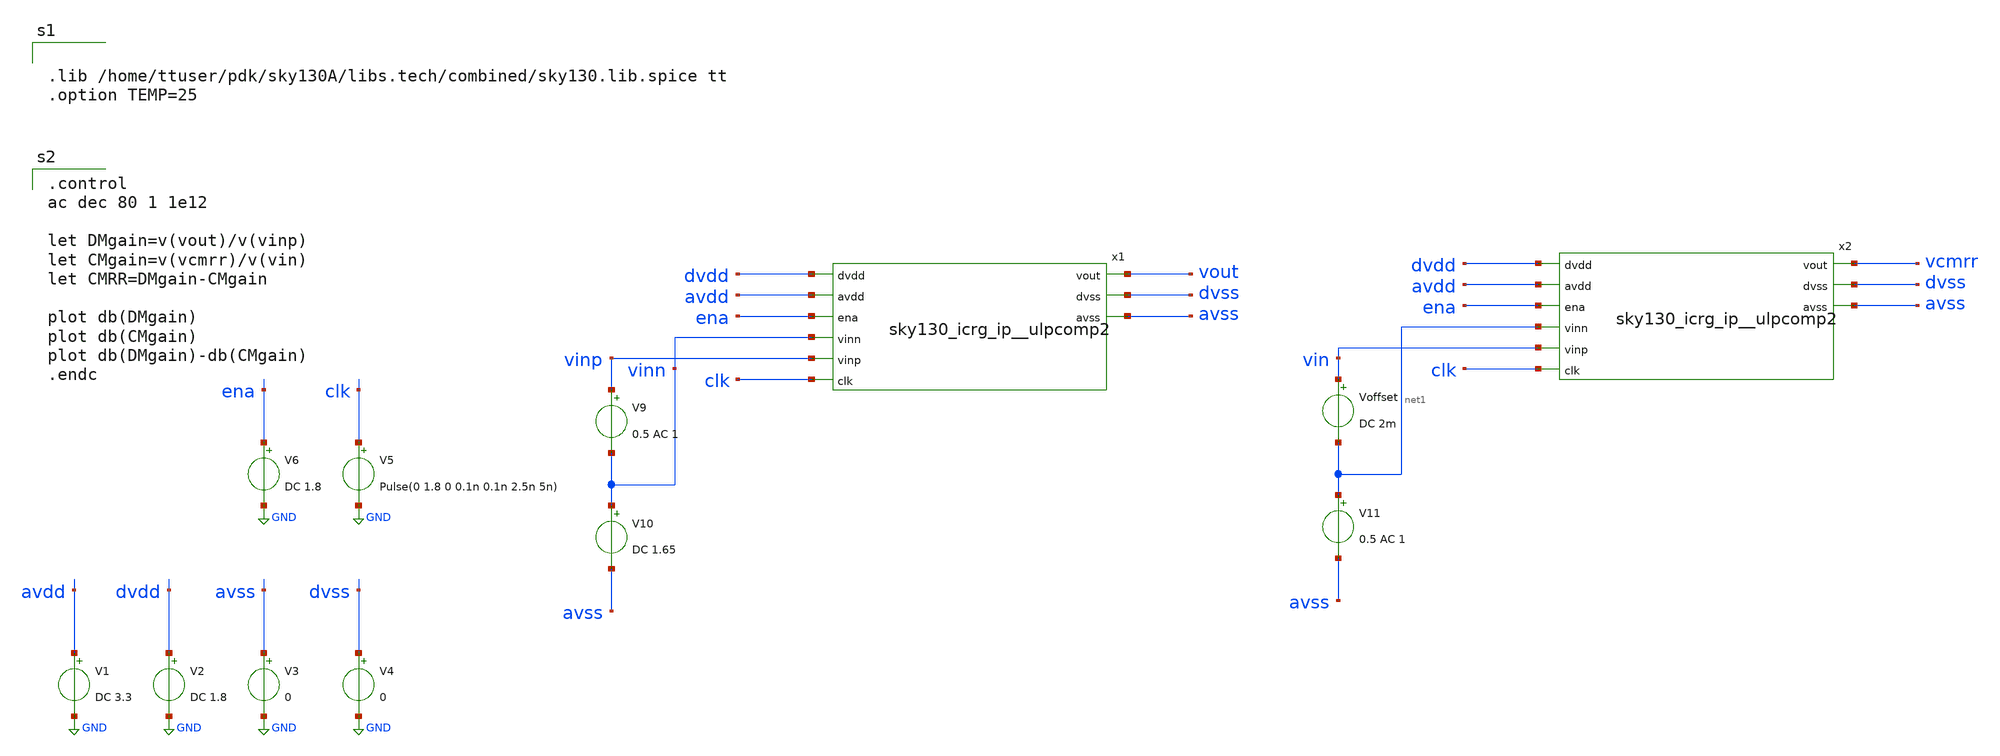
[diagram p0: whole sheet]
** sch_path: xschem/CMRR_tb.sch
**.subckt CMRR_tb
x1 dvdd avdd ena vout vinn vinp clk dvss avss sky130_icrg_ip__ulpcomp2
V1 avdd GND DC 3.3
V2 dvdd GND DC 1.8
V3 avss GND 0
V4 dvss GND 0
V5 clk GND Pulse(0 1.8 0 0.1n 0.1n 2.5n 5n)
V6 ena GND DC 1.8
V9 vinp vinn 0.5 AC 1
V10 vinn avss DC 1.65
x2 dvdd avdd ena vcmrr net1 vin clk dvss avss sky130_icrg_ip__ulpcomp2
V11 net1 avss 0.5 AC 1
Voffset vin net1 DC 2m
**** begin user architecture code


.lib /home/ttuser/pdk/sky130A/libs.tech/combined/sky130.lib.spice tt
.option TEMP=25


.control
ac dec 80 1 1e12

let DMgain=v(vout)/v(vinp)
let CMgain=v(vcmrr)/v(vin)
let CMRR=DMgain-CMgain

plot db(DMgain)
plot db(CMgain)
plot db(DMgain)-db(CMgain)
.endc

**** end user architecture code
**.ends

* expanding   symbol:  sky130_icrg_ip__ulpcomp2.sym # of pins=9
** sym_path: xschem/sky130_icrg_ip__ulpcomp2.sym
** sch_path: xschem/sky130_icrg_ip__ulpcomp2.sch
.subckt sky130_icrg_ip__ulpcomp2 dvdd avdd ena vout vinn vinp clk dvss avss
*.ipin avdd
*.ipin vinp
*.ipin vinn
*.opin avss
*.opin vout
*.opin dvss
*.ipin dvdd
*.ipin clk
*.ipin ena
XM1 net1 clka net3 net3 sky130_fd_pr__pfet_g5v0d10v5 L=0.5 W=3 nf=1 ad='int((nf+1)/2) * W/nf * 0.29'
+ as='int((nf+2)/2) * W/nf * 0.29' pd='2*int((nf+1)/2) * (W/nf + 0.29)' ps='2*int((nf+2)/2) * (W/nf + 0.29)'
+ nrd='0.29 / W' nrs='0.29 / W' sa=0 sb=0 sd=0 mult=1 m=1
XM2 oneg vinp net1 net1 sky130_fd_pr__pfet_g5v0d10v5 L=0.5 W=3 nf=1 ad='int((nf+1)/2) * W/nf * 0.29'
+ as='int((nf+2)/2) * W/nf * 0.29' pd='2*int((nf+1)/2) * (W/nf + 0.29)' ps='2*int((nf+2)/2) * (W/nf + 0.29)'
+ nrd='0.29 / W' nrs='0.29 / W' sa=0 sb=0 sd=0 mult=1 m=1
XM3 opos vinn net1 net1 sky130_fd_pr__pfet_g5v0d10v5 L=0.5 W=3 nf=1 ad='int((nf+1)/2) * W/nf * 0.29'
+ as='int((nf+2)/2) * W/nf * 0.29' pd='2*int((nf+1)/2) * (W/nf + 0.29)' ps='2*int((nf+2)/2) * (W/nf + 0.29)'
+ nrd='0.29 / W' nrs='0.29 / W' sa=0 sb=0 sd=0 mult=1 m=1
XM7 oneg clka net2 net2 sky130_fd_pr__nfet_03v3_nvt L=0.5 W=3 nf=1 ad='int((nf+1)/2) * W/nf * 0.29' as='int((nf+2)/2) * W/nf * 0.29'
+ pd='2*int((nf+1)/2) * (W/nf + 0.29)' ps='2*int((nf+2)/2) * (W/nf + 0.29)' nrd='0.29 / W' nrs='0.29 / W'
+ sa=0 sb=0 sd=0 mult=1 m=1
XM5 opos clka net2 net2 sky130_fd_pr__nfet_03v3_nvt L=0.5 W=3 nf=1 ad='int((nf+1)/2) * W/nf * 0.29' as='int((nf+2)/2) * W/nf * 0.29'
+ pd='2*int((nf+1)/2) * (W/nf + 0.29)' ps='2*int((nf+2)/2) * (W/nf + 0.29)' nrd='0.29 / W' nrs='0.29 / W'
+ sa=0 sb=0 sd=0 mult=1 m=1
XM6 clka clk dvss dvss sky130_fd_pr__nfet_01v8 L=0.15 W=1 nf=1 ad='int((nf+1)/2) * W/nf * 0.29' as='int((nf+2)/2) * W/nf * 0.29'
+ pd='2*int((nf+1)/2) * (W/nf + 0.29)' ps='2*int((nf+2)/2) * (W/nf + 0.29)' nrd='0.29 / W' nrs='0.29 / W'
+ sa=0 sb=0 sd=0 mult=1 m=1
XM8 clka clk dvddb dvddb sky130_fd_pr__pfet_01v8 L=0.15 W=1 nf=1 ad='int((nf+1)/2) * W/nf * 0.29' as='int((nf+2)/2) * W/nf * 0.29'
+ pd='2*int((nf+1)/2) * (W/nf + 0.29)' ps='2*int((nf+2)/2) * (W/nf + 0.29)' nrd='0.29 / W' nrs='0.29 / W'
+ sa=0 sb=0 sd=0 mult=1 m=1
XM9 net4 clkb dvddb dvddb sky130_fd_pr__pfet_01v8 L=0.15 W=1 nf=1 ad='int((nf+1)/2) * W/nf * 0.29' as='int((nf+2)/2) * W/nf * 0.29'
+ pd='2*int((nf+1)/2) * (W/nf + 0.29)' ps='2*int((nf+2)/2) * (W/nf + 0.29)' nrd='0.29 / W' nrs='0.29 / W'
+ sa=0 sb=0 sd=0 mult=1 m=1
XM10 net4 net5 dvddb dvddb sky130_fd_pr__pfet_01v8 L=0.15 W=1 nf=1 ad='int((nf+1)/2) * W/nf * 0.29' as='int((nf+2)/2) * W/nf * 0.29'
+ pd='2*int((nf+1)/2) * (W/nf + 0.29)' ps='2*int((nf+2)/2) * (W/nf + 0.29)' nrd='0.29 / W' nrs='0.29 / W'
+ sa=0 sb=0 sd=0 mult=1 m=1
XM11 net5 net4 dvddb dvddb sky130_fd_pr__pfet_01v8 L=0.15 W=1 nf=1 ad='int((nf+1)/2) * W/nf * 0.29' as='int((nf+2)/2) * W/nf * 0.29'
+ pd='2*int((nf+1)/2) * (W/nf + 0.29)' ps='2*int((nf+2)/2) * (W/nf + 0.29)' nrd='0.29 / W' nrs='0.29 / W'
+ sa=0 sb=0 sd=0 mult=1 m=1
XM12 net5 clkb dvddb dvddb sky130_fd_pr__pfet_01v8 L=0.15 W=1 nf=1 ad='int((nf+1)/2) * W/nf * 0.29' as='int((nf+2)/2) * W/nf * 0.29'
+ pd='2*int((nf+1)/2) * (W/nf + 0.29)' ps='2*int((nf+2)/2) * (W/nf + 0.29)' nrd='0.29 / W' nrs='0.29 / W'
+ sa=0 sb=0 sd=0 mult=1 m=1
XM13 net4 opos net6 dvss sky130_fd_pr__nfet_01v8 L=0.15 W=1 nf=1 ad='int((nf+1)/2) * W/nf * 0.29' as='int((nf+2)/2) * W/nf * 0.29'
+ pd='2*int((nf+1)/2) * (W/nf + 0.29)' ps='2*int((nf+2)/2) * (W/nf + 0.29)' nrd='0.29 / W' nrs='0.29 / W'
+ sa=0 sb=0 sd=0 mult=1 m=1
XM14 net5 oneg net7 dvss sky130_fd_pr__nfet_01v8 L=0.15 W=1 nf=1 ad='int((nf+1)/2) * W/nf * 0.29' as='int((nf+2)/2) * W/nf * 0.29'
+ pd='2*int((nf+1)/2) * (W/nf + 0.29)' ps='2*int((nf+2)/2) * (W/nf + 0.29)' nrd='0.29 / W' nrs='0.29 / W'
+ sa=0 sb=0 sd=0 mult=1 m=1
XM15 net6 net5 net8 dvss sky130_fd_pr__nfet_01v8 L=0.15 W=1 nf=1 ad='int((nf+1)/2) * W/nf * 0.29' as='int((nf+2)/2) * W/nf * 0.29'
+ pd='2*int((nf+1)/2) * (W/nf + 0.29)' ps='2*int((nf+2)/2) * (W/nf + 0.29)' nrd='0.29 / W' nrs='0.29 / W'
+ sa=0 sb=0 sd=0 mult=1 m=1
XM16 net7 net4 net8 dvss sky130_fd_pr__nfet_01v8 L=0.15 W=1 nf=1 ad='int((nf+1)/2) * W/nf * 0.29' as='int((nf+2)/2) * W/nf * 0.29'
+ pd='2*int((nf+1)/2) * (W/nf + 0.29)' ps='2*int((nf+2)/2) * (W/nf + 0.29)' nrd='0.29 / W' nrs='0.29 / W'
+ sa=0 sb=0 sd=0 mult=1 m=1
XM17 net8 clkb dvss dvss sky130_fd_pr__nfet_01v8 L=0.15 W=1 nf=1 ad='int((nf+1)/2) * W/nf * 0.29' as='int((nf+2)/2) * W/nf * 0.29'
+ pd='2*int((nf+1)/2) * (W/nf + 0.29)' ps='2*int((nf+2)/2) * (W/nf + 0.29)' nrd='0.29 / W' nrs='0.29 / W'
+ sa=0 sb=0 sd=0 mult=1 m=1
XM4 net2 net2 avss avss sky130_fd_pr__nfet_03v3_nvt L=0.5 W=3 nf=1 ad='int((nf+1)/2) * W/nf * 0.29' as='int((nf+2)/2) * W/nf * 0.29'
+ pd='2*int((nf+1)/2) * (W/nf + 0.29)' ps='2*int((nf+2)/2) * (W/nf + 0.29)' nrd='0.29 / W' nrs='0.29 / W'
+ sa=0 sb=0 sd=0 mult=1 m=1
XM18 vout net4 dvss dvss sky130_fd_pr__nfet_01v8 L=0.15 W=1 nf=1 ad='int((nf+1)/2) * W/nf * 0.29' as='int((nf+2)/2) * W/nf * 0.29'
+ pd='2*int((nf+1)/2) * (W/nf + 0.29)' ps='2*int((nf+2)/2) * (W/nf + 0.29)' nrd='0.29 / W' nrs='0.29 / W'
+ sa=0 sb=0 sd=0 mult=1 m=1
XM19 vout net4 dvdd dvdd sky130_fd_pr__pfet_01v8 L=0.15 W=1 nf=1 ad='int((nf+1)/2) * W/nf * 0.29' as='int((nf+2)/2) * W/nf * 0.29'
+ pd='2*int((nf+1)/2) * (W/nf + 0.29)' ps='2*int((nf+2)/2) * (W/nf + 0.29)' nrd='0.29 / W' nrs='0.29 / W'
+ sa=0 sb=0 sd=0 mult=1 m=1
XM20 avdd ena net3 avss sky130_fd_pr__nfet_03v3_nvt L=0.5 W=3 nf=1 ad='int((nf+1)/2) * W/nf * 0.29' as='int((nf+2)/2) * W/nf * 0.29'
+ pd='2*int((nf+1)/2) * (W/nf + 0.29)' ps='2*int((nf+2)/2) * (W/nf + 0.29)' nrd='0.29 / W' nrs='0.29 / W'
+ sa=0 sb=0 sd=0 mult=1 m=1
XM23 dvdd ena dvddb dvss sky130_fd_pr__nfet_01v8 L=0.15 W=1 nf=1 ad='int((nf+1)/2) * W/nf * 0.29' as='int((nf+2)/2) * W/nf * 0.29'
+ pd='2*int((nf+1)/2) * (W/nf + 0.29)' ps='2*int((nf+2)/2) * (W/nf + 0.29)' nrd='0.29 / W' nrs='0.29 / W'
+ sa=0 sb=0 sd=0 mult=1 m=1
XM21 clkb clka dvss dvss sky130_fd_pr__nfet_01v8 L=0.15 W=1 nf=1 ad='int((nf+1)/2) * W/nf * 0.29' as='int((nf+2)/2) * W/nf * 0.29'
+ pd='2*int((nf+1)/2) * (W/nf + 0.29)' ps='2*int((nf+2)/2) * (W/nf + 0.29)' nrd='0.29 / W' nrs='0.29 / W'
+ sa=0 sb=0 sd=0 mult=1 m=1
XM22 clkb clka dvddb dvddb sky130_fd_pr__pfet_01v8 L=0.15 W=1 nf=1 ad='int((nf+1)/2) * W/nf * 0.29' as='int((nf+2)/2) * W/nf * 0.29'
+ pd='2*int((nf+1)/2) * (W/nf + 0.29)' ps='2*int((nf+2)/2) * (W/nf + 0.29)' nrd='0.29 / W' nrs='0.29 / W'
+ sa=0 sb=0 sd=0 mult=1 m=1
.ends

.GLOBAL GND
.end
